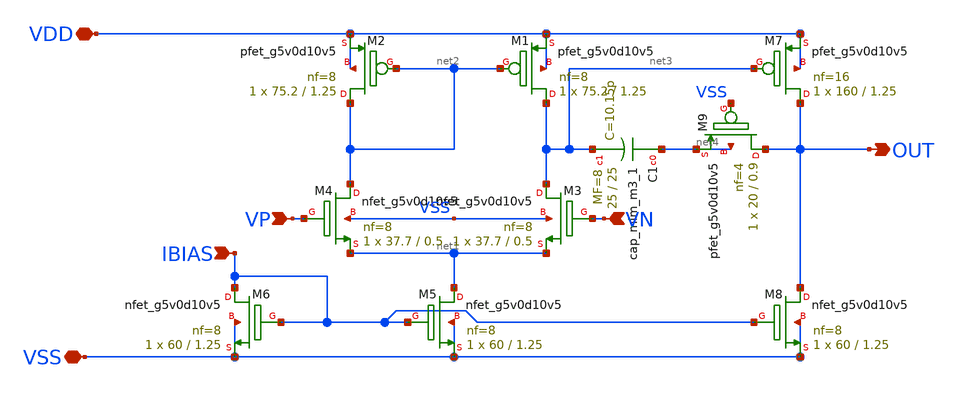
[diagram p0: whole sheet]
** sch_path: xschem/error-amplifier/schematics/two-stage-miller.sch
**.subckt two-stage-miller VDD VSS IBIAS VP VN OUT
*.iopin VDD
*.iopin VSS
*.ipin IBIAS
*.ipin VP
*.ipin VN
*.opin OUT
XM1 net3 net2 VDD VDD sky130_fd_pr__pfet_g5v0d10v5 L=1.25 W=75.2 nf=8 ad='int((nf+1)/2) * W/nf * 0.29'
+ as='int((nf+2)/2) * W/nf * 0.29' pd='2*int((nf+1)/2) * (W/nf + 0.29)' ps='2*int((nf+2)/2) * (W/nf + 0.29)'
+ nrd='0.29 / W' nrs='0.29 / W' sa=0 sb=0 sd=0 mult=1 m=1
XM2 net2 net2 VDD VDD sky130_fd_pr__pfet_g5v0d10v5 L=1.25 W=75.2 nf=8 ad='int((nf+1)/2) * W/nf * 0.29'
+ as='int((nf+2)/2) * W/nf * 0.29' pd='2*int((nf+1)/2) * (W/nf + 0.29)' ps='2*int((nf+2)/2) * (W/nf + 0.29)'
+ nrd='0.29 / W' nrs='0.29 / W' sa=0 sb=0 sd=0 mult=1 m=1
XM3 net3 VN net1 VSS sky130_fd_pr__nfet_g5v0d10v5 L=0.5 W=37.7 nf=8 ad='int((nf+1)/2) * W/nf * 0.29'
+ as='int((nf+2)/2) * W/nf * 0.29' pd='2*int((nf+1)/2) * (W/nf + 0.29)' ps='2*int((nf+2)/2) * (W/nf + 0.29)'
+ nrd='0.29 / W' nrs='0.29 / W' sa=0 sb=0 sd=0 mult=1 m=1
XM4 net2 VP net1 VSS sky130_fd_pr__nfet_g5v0d10v5 L=0.5 W=37.7 nf=8 ad='int((nf+1)/2) * W/nf * 0.29'
+ as='int((nf+2)/2) * W/nf * 0.29' pd='2*int((nf+1)/2) * (W/nf + 0.29)' ps='2*int((nf+2)/2) * (W/nf + 0.29)'
+ nrd='0.29 / W' nrs='0.29 / W' sa=0 sb=0 sd=0 mult=1 m=1
XM5 net1 IBIAS VSS VSS sky130_fd_pr__nfet_g5v0d10v5 L=1.25 W=60 nf=8 ad='int((nf+1)/2) * W/nf * 0.29'
+ as='int((nf+2)/2) * W/nf * 0.29' pd='2*int((nf+1)/2) * (W/nf + 0.29)' ps='2*int((nf+2)/2) * (W/nf + 0.29)'
+ nrd='0.29 / W' nrs='0.29 / W' sa=0 sb=0 sd=0 mult=1 m=1
XM6 IBIAS IBIAS VSS VSS sky130_fd_pr__nfet_g5v0d10v5 L=1.25 W=60 nf=8 ad='int((nf+1)/2) * W/nf * 0.29'
+ as='int((nf+2)/2) * W/nf * 0.29' pd='2*int((nf+1)/2) * (W/nf + 0.29)' ps='2*int((nf+2)/2) * (W/nf + 0.29)'
+ nrd='0.29 / W' nrs='0.29 / W' sa=0 sb=0 sd=0 mult=1 m=1
XM7 OUT net3 VDD VDD sky130_fd_pr__pfet_g5v0d10v5 L=1.25 W=160 nf=16 ad='int((nf+1)/2) * W/nf * 0.29'
+ as='int((nf+2)/2) * W/nf * 0.29' pd='2*int((nf+1)/2) * (W/nf + 0.29)' ps='2*int((nf+2)/2) * (W/nf + 0.29)'
+ nrd='0.29 / W' nrs='0.29 / W' sa=0 sb=0 sd=0 mult=1 m=1
XM8 OUT IBIAS VSS VSS sky130_fd_pr__nfet_g5v0d10v5 L=1.25 W=60 nf=8 ad='int((nf+1)/2) * W/nf * 0.29'
+ as='int((nf+2)/2) * W/nf * 0.29' pd='2*int((nf+1)/2) * (W/nf + 0.29)' ps='2*int((nf+2)/2) * (W/nf + 0.29)'
+ nrd='0.29 / W' nrs='0.29 / W' sa=0 sb=0 sd=0 mult=1 m=1
XC1 net4 net3 sky130_fd_pr__cap_mim_m3_1 W=25 L=25 MF=8 m=8
XM9 OUT VSS net4 net4 sky130_fd_pr__pfet_g5v0d10v5 L=0.9 W=20 nf=4 ad='int((nf+1)/2) * W/nf * 0.29' as='int((nf+2)/2) * W/nf * 0.29'
+ pd='2*int((nf+1)/2) * (W/nf + 0.29)' ps='2*int((nf+2)/2) * (W/nf + 0.29)' nrd='0.29 / W' nrs='0.29 / W'
+ sa=0 sb=0 sd=0 mult=1 m=1
**.ends
.end
